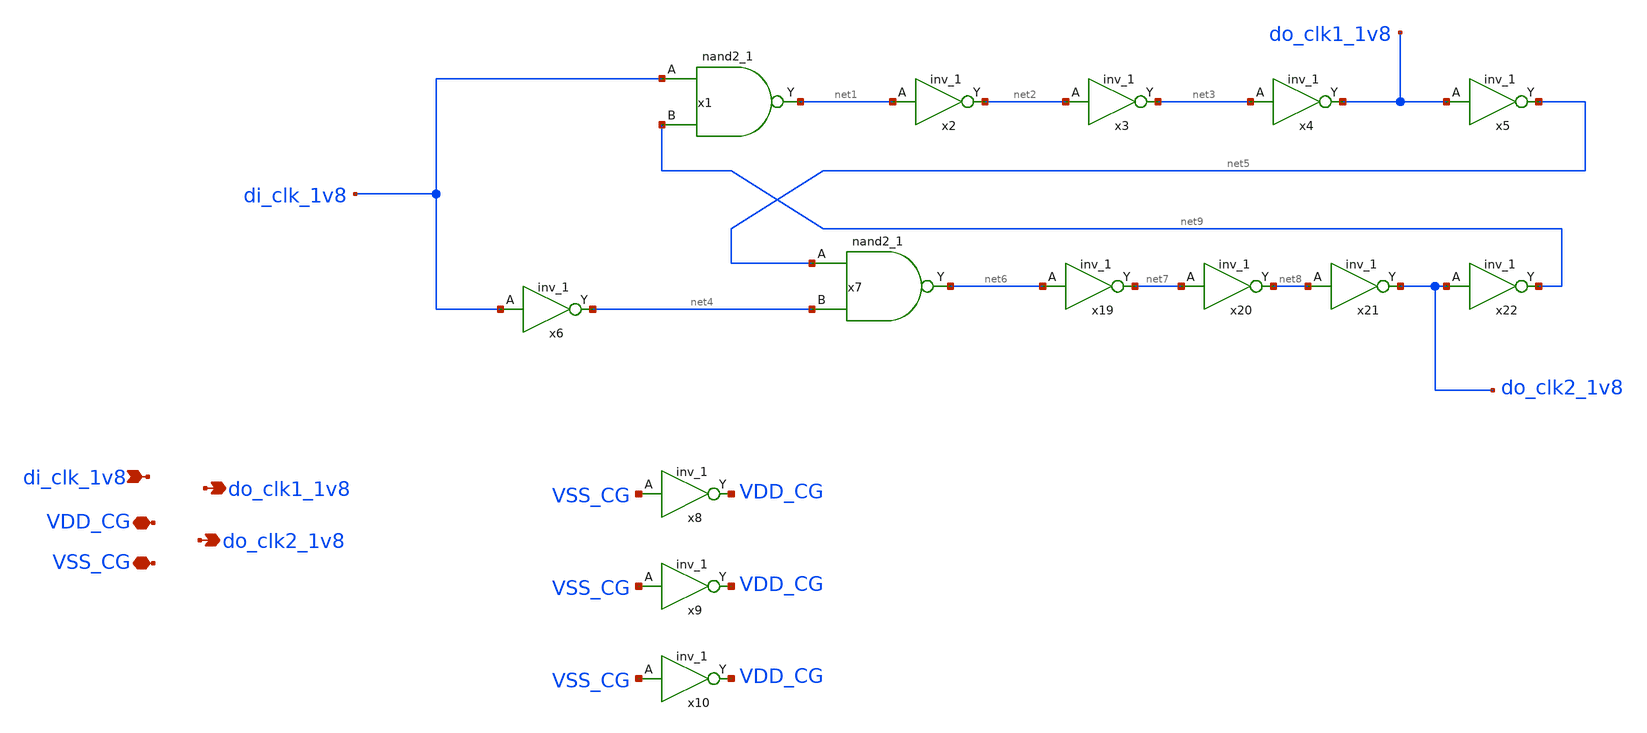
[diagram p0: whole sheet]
** sch_path: magic/clock_generator.sch
**.subckt clock_generator di_clk_1v8 do_clk1_1v8 do_clk2_1v8 VSS_CG VDD_CG
*.ipin di_clk_1v8
*.opin do_clk1_1v8
*.opin do_clk2_1v8
*.iopin VSS_CG
*.iopin VDD_CG
x1 di_clk_1v8 net9 VSS_CG VSS_CG VDD_CG VDD_CG net1 sky130_fd_sc_hd__nand2_1
x2 net1 VSS_CG VSS_CG VDD_CG VDD_CG net2 sky130_fd_sc_hd__inv_1
x3 net2 VSS_CG VSS_CG VDD_CG VDD_CG net3 sky130_fd_sc_hd__inv_1
x4 net3 VSS_CG VSS_CG VDD_CG VDD_CG do_clk1_1v8 sky130_fd_sc_hd__inv_1
x5 do_clk1_1v8 VSS_CG VSS_CG VDD_CG VDD_CG net5 sky130_fd_sc_hd__inv_1
x6 di_clk_1v8 VSS_CG VSS_CG VDD_CG VDD_CG net4 sky130_fd_sc_hd__inv_1
x7 net5 net4 VSS_CG VSS_CG VDD_CG VDD_CG net6 sky130_fd_sc_hd__nand2_1
x19 net6 VSS_CG VSS_CG VDD_CG VDD_CG net7 sky130_fd_sc_hd__inv_1
x20 net7 VSS_CG VSS_CG VDD_CG VDD_CG net8 sky130_fd_sc_hd__inv_1
x21 net8 VSS_CG VSS_CG VDD_CG VDD_CG do_clk2_1v8 sky130_fd_sc_hd__inv_1
x22 do_clk2_1v8 VSS_CG VSS_CG VDD_CG VDD_CG net9 sky130_fd_sc_hd__inv_1
x8 VSS_CG VSS_CG VSS_CG VDD_CG VDD_CG VDD_CG sky130_fd_sc_hd__inv_1
x9 VSS_CG VSS_CG VSS_CG VDD_CG VDD_CG VDD_CG sky130_fd_sc_hd__inv_1
x10 VSS_CG VSS_CG VSS_CG VDD_CG VDD_CG VDD_CG sky130_fd_sc_hd__inv_1
**.ends
.end
